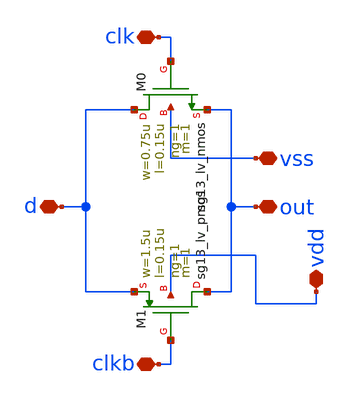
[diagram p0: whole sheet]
** sch_path: design/blocks/transmissiongate/schematic/transmissiongate.sch
**.subckt transmissiongate out d clkb clk vdd vss
*.iopin out
*.iopin d
*.iopin clkb
*.iopin clk
*.iopin vdd
*.iopin vss
XM1 out clkb d vdd sg13_lv_pmos w=1.5u l=0.15u ng=1 m=1 mm_ok=1
XM0 d clk out vss sg13_lv_nmos w=0.75u l=0.15u ng=1 m=1 mm_ok=1
**.ends
.end
